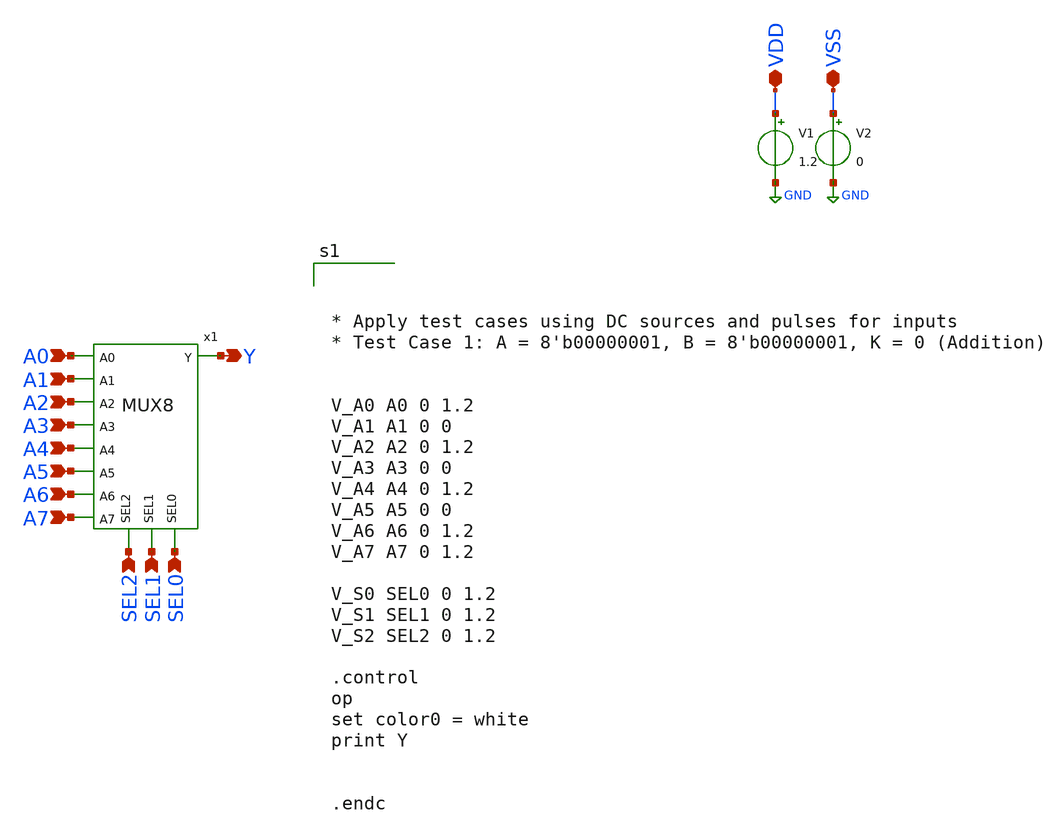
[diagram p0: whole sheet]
** sch_path: design/xschem/TEST_BENCHES/MUX8_RSHIFT_TB.sch
**.subckt MUX8_RSHIFT_TB A0 A1 Y VDD VSS SEL0 SEL1 SEL2 A2 A3 A4 A5 A6 A7
*.ipin A0
*.ipin A1
*.opin Y
*.iopin VDD
*.iopin VSS
*.ipin SEL0
*.ipin SEL1
*.ipin SEL2
*.ipin A2
*.ipin A3
*.ipin A4
*.ipin A5
*.ipin A6
*.ipin A7
V1 VDD GND 1.2
V2 VSS GND 0
x1 SEL0 SEL1 SEL2 A0 A1 A2 A3 A4 A5 Y A6 A7 MUX8
**** begin user architecture code

** opencircuitdesign pdks install
.lib $::SKYWATER_MODELS/sky130.lib.spice tt_mm





* Apply test cases using DC sources and pulses for inputs
* Test Case 1: A = 8'b00000001, B = 8'b00000001, K = 0 (Addition)


V_A0 A0 0 1.2
V_A1 A1 0 0
V_A2 A2 0 1.2
V_A3 A3 0 0
V_A4 A4 0 1.2
V_A5 A5 0 0
V_A6 A6 0 1.2
V_A7 A7 0 1.2

V_S0 SEL0 0 1.2
V_S1 SEL1 0 1.2
V_S2 SEL2 0 1.2

.control
op
set color0 = white
print Y


.endc


**** end user architecture code
**.ends
.GLOBAL GND
.end
